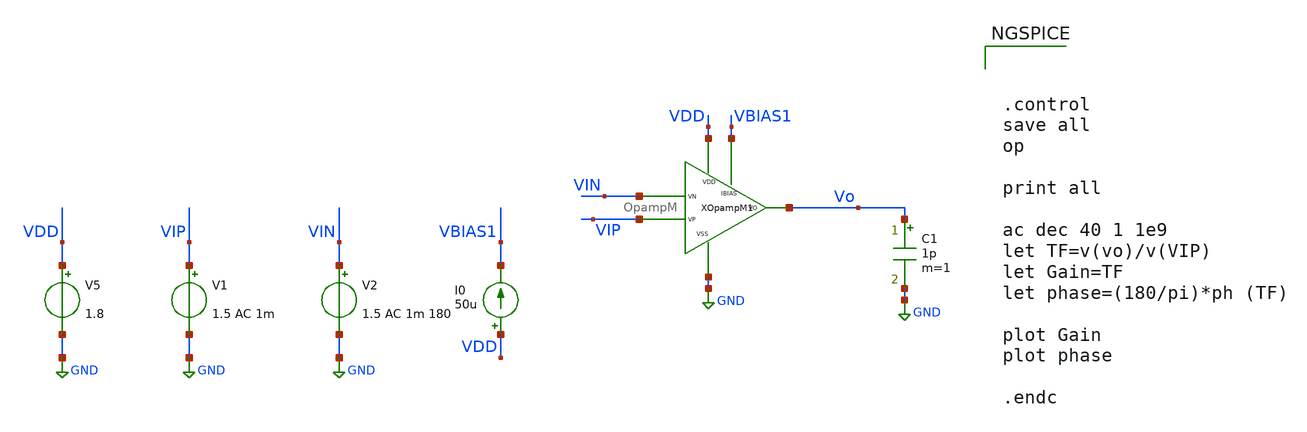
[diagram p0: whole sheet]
** sch_path: xschem/xschem_BGR_Top/Op_Amp/OpampM_tb_ac.sch
**.subckt OpampM_tb_ac
V1 VIP GND 1.5 AC 1m
V2 VIN GND 1.5 AC 1m 180
V5 VDD GND 1.8
I0 VDD VBIAS1 50u
C1 Vo GND 1p m=1
XOpampM1 VBIAS1 VDD VIN VIP GND Vo OpampM
**** begin user architecture code



.control
save all
op

print all

ac dec 40 1 1e9
let TF=v(vo)/v(VIP)
let Gain=TF
let phase=(180/pi)*ph (TF)

plot Gain
plot phase

.endc


** manual skywater pdks install (with patches applied)
* .lib $::SKYWATER_MODELS/models/sky130.lib.spice tt

** opencircuitdesign pdks install
.lib $::SKYWATER_MODELS/sky130.lib.spice tt


**** end user architecture code
**.ends

* expanding   symbol:  Sigma_Delta/Op_Amp/OpampM.sym # of pins=6
** sym_path: xschem/xschem_BGR_Top/Op_Amp/OpampM.sym
** sch_path: xschem/xschem_BGR_Top/Op_Amp/OpampM.sch
.subckt OpampM IBIAS VDD VN VP VSS VO
*.iopin VDD
*.iopin VSS
*.iopin VP
*.iopin VN
*.iopin VO
*.iopin IBIAS
XM1 net1 VN net3 VSS sky130_fd_pr__nfet_01v8 L=0.5 W=50 nf=10 ad='int((nf+1)/2) * W/nf * 0.29' as='int((nf+2)/2) * W/nf * 0.29'
+ pd='2*int((nf+1)/2) * (W/nf + 0.29)' ps='2*int((nf+2)/2) * (W/nf + 0.29)' nrd='0.29 / W' nrs='0.29 / W'
+ sa=0 sb=0 sd=0 mult=1 m=1
XM3 net1 net1 VDD VDD sky130_fd_pr__pfet_01v8_lvt L=0.5 W=60 nf=10 ad='int((nf+1)/2) * W/nf * 0.29' as='int((nf+2)/2) * W/nf * 0.29'
+ pd='2*int((nf+1)/2) * (W/nf + 0.29)' ps='2*int((nf+2)/2) * (W/nf + 0.29)' nrd='0.29 / W' nrs='0.29 / W'
+ sa=0 sb=0 sd=0 mult=1 m=1
XM2 net2 VP net3 VSS sky130_fd_pr__nfet_01v8 L=0.5 W=50 nf=10 ad='int((nf+1)/2) * W/nf * 0.29' as='int((nf+2)/2) * W/nf * 0.29'
+ pd='2*int((nf+1)/2) * (W/nf + 0.29)' ps='2*int((nf+2)/2) * (W/nf + 0.29)' nrd='0.29 / W' nrs='0.29 / W'
+ sa=0 sb=0 sd=0 mult=1 m=1
XM4 net2 net1 VDD VDD sky130_fd_pr__pfet_01v8_lvt L=0.5 W=60 nf=10 ad='int((nf+1)/2) * W/nf * 0.29' as='int((nf+2)/2) * W/nf * 0.29'
+ pd='2*int((nf+1)/2) * (W/nf + 0.29)' ps='2*int((nf+2)/2) * (W/nf + 0.29)' nrd='0.29 / W' nrs='0.29 / W'
+ sa=0 sb=0 sd=0 mult=1 m=1
XM5 net3 IBIAS VSS VSS sky130_fd_pr__nfet_01v8 L=0.5 W=21 nf=10 ad='int((nf+1)/2) * W/nf * 0.29' as='int((nf+2)/2) * W/nf * 0.29'
+ pd='2*int((nf+1)/2) * (W/nf + 0.29)' ps='2*int((nf+2)/2) * (W/nf + 0.29)' nrd='0.29 / W' nrs='0.29 / W'
+ sa=0 sb=0 sd=0 mult=1 m=1
XM7 VO IBIAS VSS VSS sky130_fd_pr__nfet_01v8 L=0.5 W=63 nf=10 ad='int((nf+1)/2) * W/nf * 0.29' as='int((nf+2)/2) * W/nf * 0.29'
+ pd='2*int((nf+1)/2) * (W/nf + 0.29)' ps='2*int((nf+2)/2) * (W/nf + 0.29)' nrd='0.29 / W' nrs='0.29 / W'
+ sa=0 sb=0 sd=0 mult=1 m=1
XM8 IBIAS IBIAS VSS VSS sky130_fd_pr__nfet_01v8 L=0.5 W=21 nf=10 ad='int((nf+1)/2) * W/nf * 0.29' as='int((nf+2)/2) * W/nf * 0.29'
+ pd='2*int((nf+1)/2) * (W/nf + 0.29)' ps='2*int((nf+2)/2) * (W/nf + 0.29)' nrd='0.29 / W' nrs='0.29 / W'
+ sa=0 sb=0 sd=0 mult=1 m=1
XC1 net2 VO sky130_fd_pr__cap_mim_m3_1 W=24 L=24 MF=1 m=1
XC2 VDD VSS sky130_fd_pr__cap_mim_m3_1 W=30 L=10 MF=1 m=1
XC3 VDD VSS sky130_fd_pr__cap_mim_m3_1 W=30 L=10 MF=1 m=1
XM6 VO net2 VDD VDD sky130_fd_pr__pfet_01v8_lvt L=0.50 W=355 nf=20 ad='int((nf+1)/2) * W/nf * 0.29' as='int((nf+2)/2) * W/nf * 0.29'
+ pd='2*int((nf+1)/2) * (W/nf + 0.29)' ps='2*int((nf+2)/2) * (W/nf + 0.29)' nrd='0.29 / W' nrs='0.29 / W'
+ sa=0 sb=0 sd=0 mult=1 m=1
.ends

.GLOBAL GND
.end
